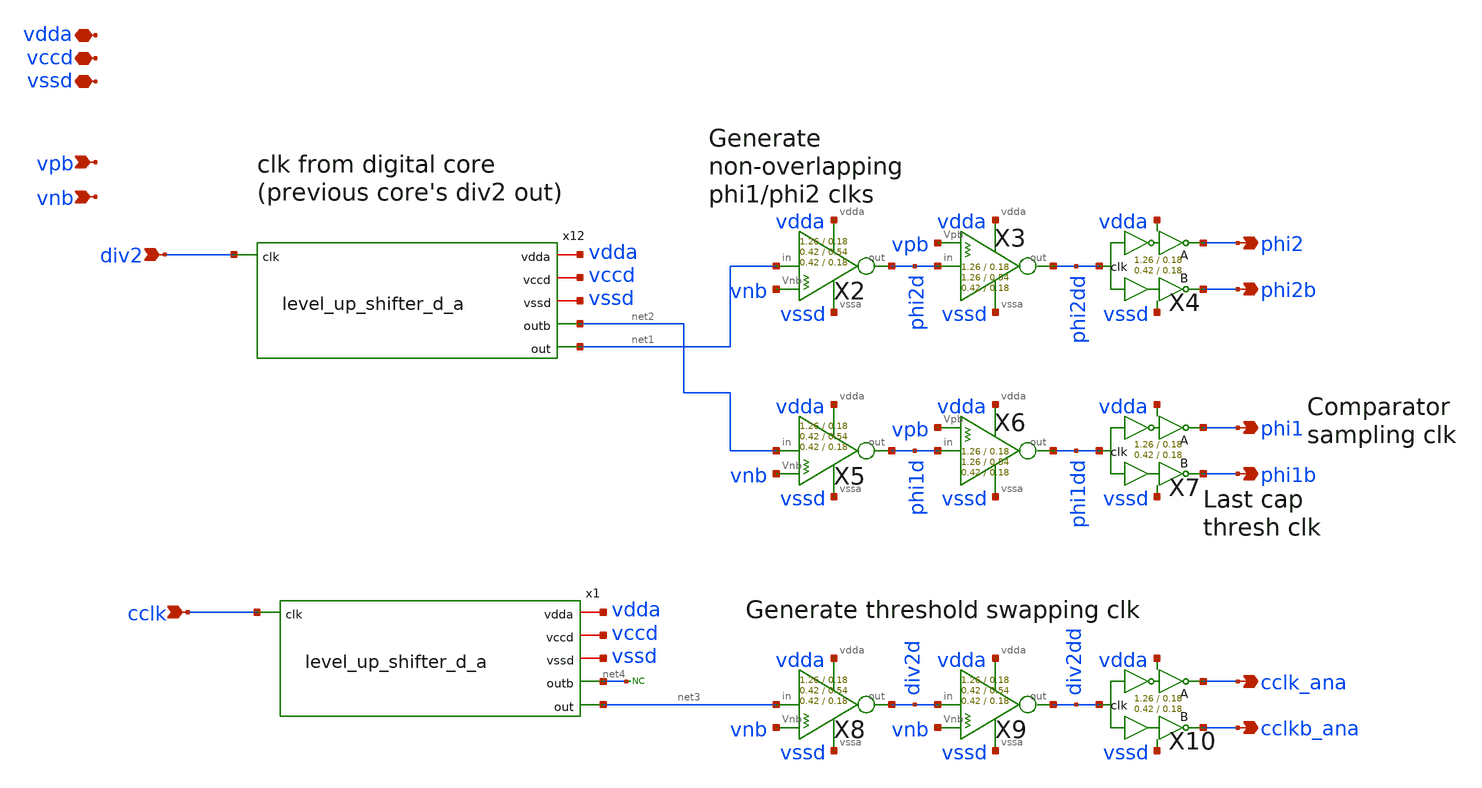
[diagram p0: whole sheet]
** sch_path: xschem/clkgen/filter_clkgen_balanced_clks.sch
**.subckt filter_clkgen_balanced_clks div2 phi2 phi2b phi1 phi1b cclk_ana cclkb_ana vpb vnb cclk
*+ vdda vccd vssd
*.ipin div2
*.opin phi2
*.opin phi2b
*.opin phi1
*.opin phi1b
*.opin cclk_ana
*.opin cclkb_ana
*.ipin vpb
*.ipin vnb
*.ipin cclk
*.iopin vdda
*.iopin vccd
*.iopin vssd
X4 phi2dd phi2 phi2b vdda vssd comp_clks Wpmos=1.26 Lpmos=0.18 Wnmos=0.42 Lnmos=0.18
X7 phi1dd phi1 phi1b vdda vssd comp_clks Wpmos=1.26 Lpmos=0.18 Wnmos=0.42 Lnmos=0.18
X10 div2dd cclk_ana cclkb_ana vdda vssd comp_clks Wpmos=1.26 Lpmos=0.18 Wnmos=0.42 Lnmos=0.18
X2 net1 phi2d vnb vdda vssd inv_weak_pulldown Wpmos=1.26 Lpmos= Wnmos= Lnmos=0.54
X5 net2 phi1d vnb vdda vssd inv_weak_pulldown Wpmos=1.26 Lpmos= Wnmos= Lnmos=0.54
X8 net3 div2d vnb vdda vssd inv_weak_pulldown Wpmos=1.26 Lpmos= Wnmos= Lnmos=0.54
X9 div2d div2dd vnb vdda vssd inv_weak_pulldown Wpmos=1.26 Lpmos= Wnmos= Lnmos=0.54
X3 phi2d phi2dd vpb vdda vssd inv_weak_pullup Wpmos=1.26 Lpmos=0.54 Wnmos= Lnmos=
X6 phi1d phi1dd vpb vdda vssd inv_weak_pullup Wpmos=1.26 Lpmos=0.54 Wnmos= Lnmos=
* noconn #net4
x12 vdda vccd vssd div2 net2 net1 level_up_shifter_d_a
x1 vdda vccd vssd cclk net4 net3 level_up_shifter_d_a
**.ends
.end
